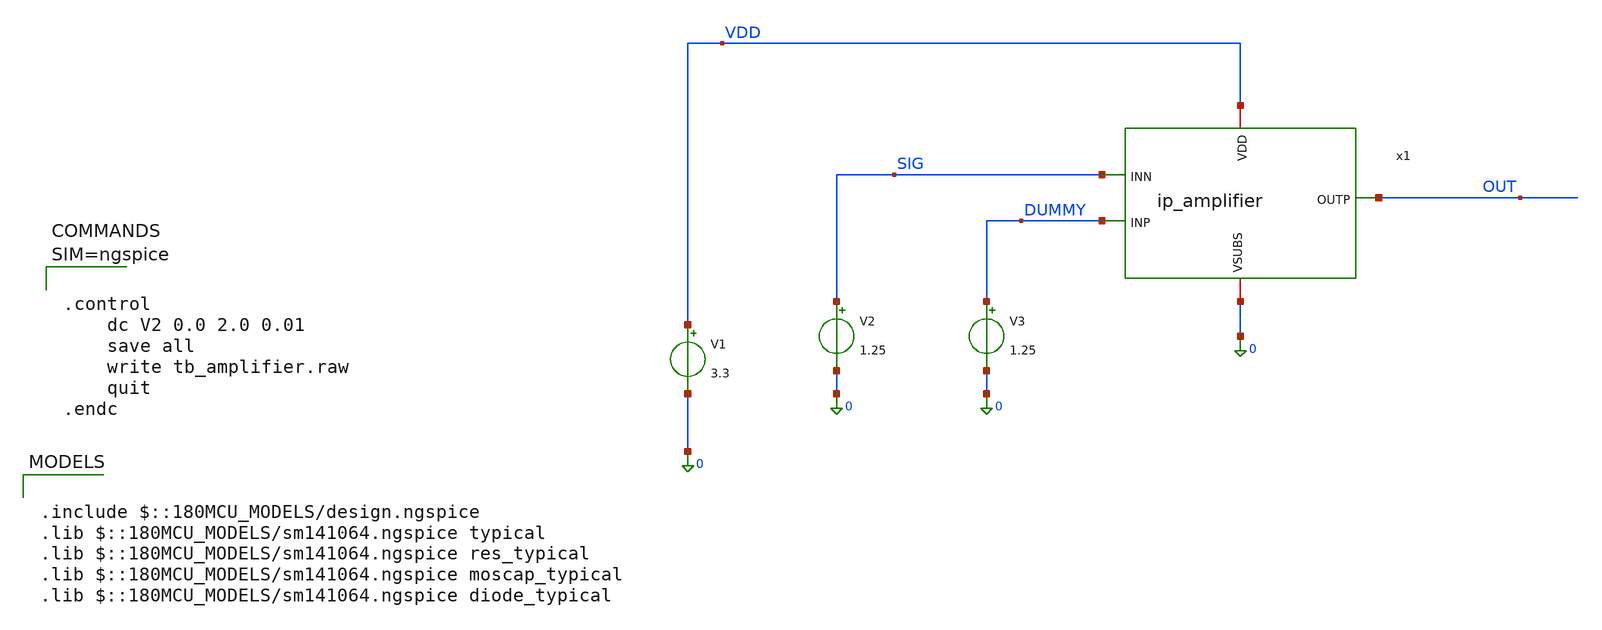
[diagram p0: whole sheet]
** sch_path: xschem/tb_amplifier.sch
**.subckt tb_amplifier
V1 VDD 0 3.3
x1 VDD OUT DUMMY SIG 0 ip_amplifier
V3 DUMMY 0 1.25
V2 SIG 0 1.25
**** begin user architecture code

.include $::180MCU_MODELS/design.ngspice
.lib $::180MCU_MODELS/sm141064.ngspice typical
.lib $::180MCU_MODELS/sm141064.ngspice res_typical
.lib $::180MCU_MODELS/sm141064.ngspice moscap_typical
.lib $::180MCU_MODELS/sm141064.ngspice diode_typical




.control
	dc V2 0.0 2.0 0.01
	save all
	write tb_amplifier.raw
	quit
.endc



**** end user architecture code
**.ends

* expanding   symbol:  ip_amplifier.sym # of pins=5
** sym_path: xschem/ip_amplifier.sym
** sch_path: xschem/ip_amplifier.sch
.subckt ip_amplifier VDD OUTP INP INN VSUBS
*.iopin VDD
*.iopin VSUBS
*.ipin INP
*.ipin INN
*.opin OUTP
XM1 OUTN INP net1 VDD pfet_03v3 L=0.5u W=15.0u nf=1 ad='int((nf+1)/2) * W/nf * 0.18u' as='int((nf+2)/2) * W/nf * 0.18u'
+ pd='2*int((nf+1)/2) * (W/nf + 0.18u)' ps='2*int((nf+2)/2) * (W/nf + 0.18u)' nrd='0.18u / W' nrs='0.18u / W'
+ sa=0 sb=0 sd=0 m=5 par=5
XM2 OUTP INN net8 VDD pfet_03v3 L=0.5u W=15.0u nf=1 ad='int((nf+1)/2) * W/nf * 0.18u' as='int((nf+2)/2) * W/nf * 0.18u'
+ pd='2*int((nf+1)/2) * (W/nf + 0.18u)' ps='2*int((nf+2)/2) * (W/nf + 0.18u)' nrd='0.18u / W' nrs='0.18u / W'
+ sa=0 sb=0 sd=0 m=5 par=5
XM5 net3 TCOM VDD VDD pfet_03v3 L=0.5u W=15.0u nf=1 ad='int((nf+1)/2) * W/nf * 0.18u' as='int((nf+2)/2) * W/nf * 0.18u'
+ pd='2*int((nf+1)/2) * (W/nf + 0.18u)' ps='2*int((nf+2)/2) * (W/nf + 0.18u)' nrd='0.18u / W' nrs='0.18u / W'
+ sa=0 sb=0 sd=0 m=3 par=3
XM3 TCOM TCOM VDD VDD pfet_03v3 L=0.5u W=15.0u nf=1 ad='int((nf+1)/2) * W/nf * 0.18u' as='int((nf+2)/2) * W/nf * 0.18u'
+ pd='2*int((nf+1)/2) * (W/nf + 0.18u)' ps='2*int((nf+2)/2) * (W/nf + 0.18u)' nrd='0.18u / W' nrs='0.18u / W'
+ sa=0 sb=0 sd=0 m=6 par=6
XR6 net6 TCOM VSUBS ppolyf_u_1k r_width=1e-6 r_length=6e-6 m=1
XR5 net5 net6 VSUBS ppolyf_u_1k r_width=1e-6 r_length=6e-6 m=1
XR7 net4 net5 VSUBS ppolyf_u_1k r_width=1e-6 r_length=6e-6 m=1
XR8 net7 net4 VSUBS ppolyf_u_1k r_width=1e-6 r_length=6e-6 m=1
Vmeas net7 VSUBS 0
Vmeas1 net3 net2 0
XR9 net8 net2 VSUBS ppolyf_u_1k r_width=1e-6 r_length=4.5e-6 m=1
XR1 net1 net2 VSUBS ppolyf_u_1k r_width=2e-6 r_length=1e-6 m=1
XR4 net10 net11 VSUBS ppolyf_u_1k r_width=1e-6 r_length=6e-6 m=1
XR2 net9 net10 VSUBS ppolyf_u_1k r_width=1e-6 r_length=6e-6 m=1
XR10 net13 OUTN VSUBS ppolyf_u_1k r_width=1e-6 r_length=6e-6 m=1
XR11 net12 net13 VSUBS ppolyf_u_1k r_width=1e-6 r_length=6e-6 m=1
XR12 VSUBS net9 VSUBS ppolyf_u_1k r_width=1e-6 r_length=6e-6 m=1
XR13 net11 net12 VSUBS ppolyf_u_1k r_width=1e-6 r_length=6e-6 m=1
XR3 net15 net16 VSUBS ppolyf_u_1k r_width=1e-6 r_length=6e-6 m=1
XR14 net14 net15 VSUBS ppolyf_u_1k r_width=1e-6 r_length=6e-6 m=1
XR15 net18 OUTP VSUBS ppolyf_u_1k r_width=1e-6 r_length=6e-6 m=1
XR16 net17 net18 VSUBS ppolyf_u_1k r_width=1e-6 r_length=6e-6 m=1
XR17 VSUBS net14 VSUBS ppolyf_u_1k r_width=1e-6 r_length=6e-6 m=1
XR18 net16 net17 VSUBS ppolyf_u_1k r_width=1e-6 r_length=6e-6 m=1
.ends

.end
